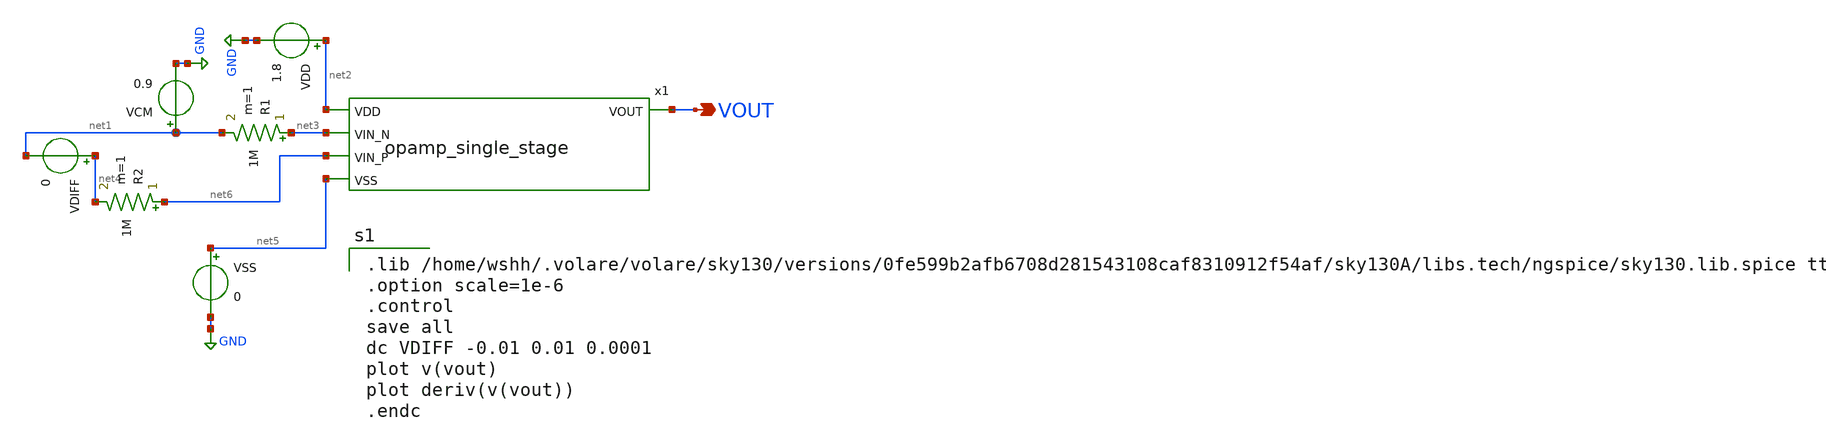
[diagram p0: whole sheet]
** sch_path: analog/schematics/tb_dc_analysis.sch
**.subckt tb_dc_analysis VOUT
*.opin VOUT
VSS net5 GND 0
VDD net2 GND 1.8
VCM net1 GND 0.9
VDIFF net4 net1 0
R1 net3 net1 1M m=1
R2 net6 net4 1M m=1
x1 VOUT net2 net3 net6 net5 opamp_single_stage
**** begin user architecture code

.lib /home/wshh/.volare/volare/sky130/versions/0fe599b2afb6708d281543108caf8310912f54af/sky130A/libs.tech/ngspice/sky130.lib.spice tt
.option scale=1e-6
.control
save all
dc VDIFF -0.01 0.01 0.0001
plot v(vout)
plot deriv(v(vout))
.endc

**** end user architecture code
**.ends

* expanding   symbol:  /home/wshh/Shiheng_Analog_Bootcamp/analog/schematics/opamp_single_stage.sym #
*+ of pins=5
** sym_path: analog/schematics/opamp_single_stage.sym
** sch_path: analog/schematics/opamp_single_stage.sch
.subckt opamp_single_stage VOUT VDD VIN_N VIN_P VSS
*.ipin VIN_P
*.ipin VIN_N
*.ipin VDD
*.ipin VSS
*.opin VOUT
XM1 net1 VIN_P net2 GND sky130_fd_pr__nfet_01v8 L=0.15 W=1 nf=1 ad='int((1 + 1)/2) * 1 / 1 * 0.29' as='int((1 + 2)/2) * 1 / 1 * 0.29'
+ pd='2*int((1 + 1)/2) * (1 / 1 + 0.29)' ps='2*int((1 + 2)/2) * (1 / 1 + 0.29)' nrd='0.29 / 1 ' nrs='0.29 / 1 '
+ sa=0 sb=0 sd=0 mult=1 m=1
XM9 VSS net3 net2 VDD sky130_fd_pr__pfet_01v8 L=0.15 W=1 nf=1 ad='int((1 + 1)/2) * 1 / 1 * 0.29' as='int((1 + 2)/2) * 1 / 1 * 0.29'
+ pd='2*int((1 + 1)/2) * (1 / 1 + 0.29)' ps='2*int((1 + 2)/2) * (1 / 1 + 0.29)' nrd='0.29 / 1 ' nrs='0.29 / 1 '
+ sa=0 sb=0 sd=0 mult=1 m=1
XM2 net2 VIN_N VOUT GND sky130_fd_pr__nfet_01v8 L=0.15 W=1 nf=1 ad='int((1 + 1)/2) * 1 / 1 * 0.29' as='int((1 + 2)/2) * 1 / 1 * 0.29'
+ pd='2*int((1 + 1)/2) * (1 / 1 + 0.29)' ps='2*int((1 + 2)/2) * (1 / 1 + 0.29)' nrd='0.29 / 1 ' nrs='0.29 / 1 '
+ sa=0 sb=0 sd=0 mult=1 m=1
XM3 VDD net1 net1 VDD sky130_fd_pr__pfet_01v8 L=0.15 W=1 nf=1 ad='int((nf+1)/2) * W/nf * 0.29' as='int((nf+2)/2) * W/nf * 0.29'
+ pd='2*int((nf+1)/2) * (W/nf + 0.29)' ps='2*int((nf+2)/2) * (W/nf + 0.29)' nrd='0.29 / W' nrs='0.29 / W'
+ sa=0 sb=0 sd=0 mult=1 m=1
XM4 VOUT net1 VDD VDD sky130_fd_pr__pfet_01v8 L=0.15 W=1 nf=1 ad='int((nf+1)/2) * W/nf * 0.29' as='int((nf+2)/2) * W/nf * 0.29'
+ pd='2*int((nf+1)/2) * (W/nf + 0.29)' ps='2*int((nf+2)/2) * (W/nf + 0.29)' nrd='0.29 / W' nrs='0.29 / W'
+ sa=0 sb=0 sd=0 mult=1 m=1
VB2 net3 net4 0.7
.ends

.GLOBAL GND
.end
